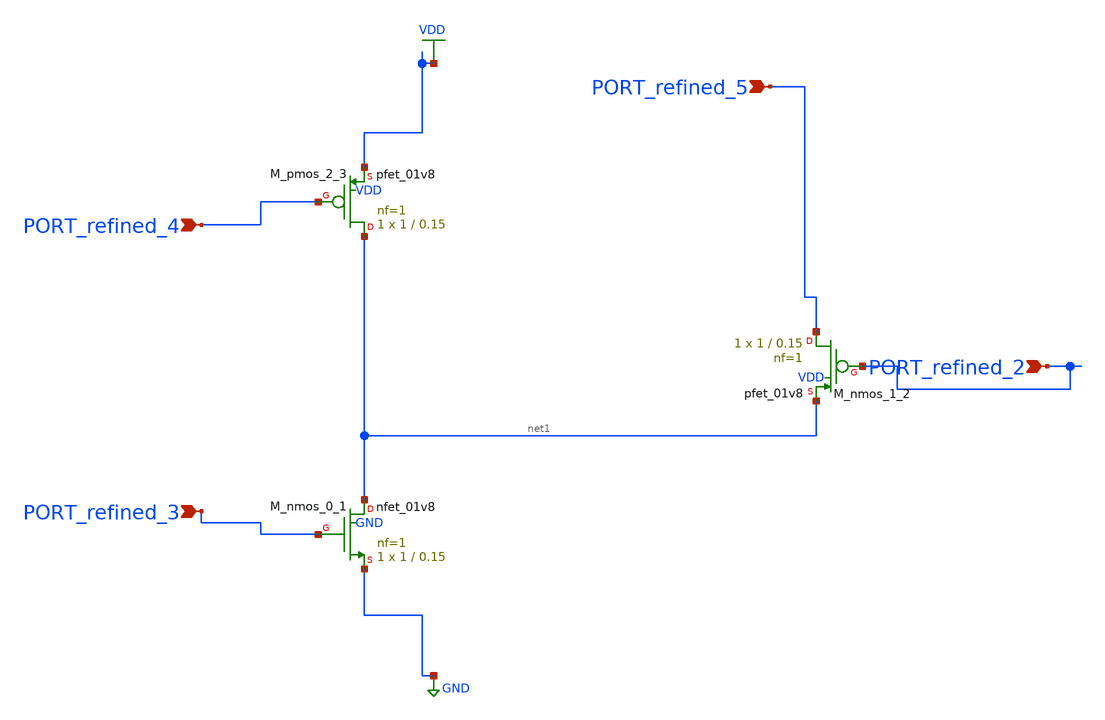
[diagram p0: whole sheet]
** sch_path: schematics/AMSNet/143.sch
**.subckt 143 PORT_refined_2 PORT_refined_3 PORT_refined_4 PORT_refined_5
*.ipin PORT_refined_2
*.ipin PORT_refined_3
*.ipin PORT_refined_4
*.ipin PORT_refined_5
XM_nmos_0_1 net1 PORT_refined_3 GND GND sky130_fd_pr__nfet_01v8 L=0.15 W=1 nf=1 ad='int((1 + 1)/2) * 1 / 1 * 0.29'
+ as='int((1 + 2)/2) * 1 / 1 * 0.29' pd='2*int((1 + 1)/2) * (1 / 1 + 0.29)' ps='2*int((1 + 2)/2) * (1 / 1 + 0.29)'
+ nrd='0.29 / 1 ' nrs='0.29 / 1 ' sa=0 sb=0 sd=0 mult=1 m=1
XM_nmos_1_2 PORT_refined_5 PORT_refined_2 net1 VDD sky130_fd_pr__pfet_01v8 L=0.15 W=1 nf=1 ad='int((1 + 1)/2) * 1 / 1 * 0.29'
+ as='int((1 + 2)/2) * 1 / 1 * 0.29' pd='2*int((1 + 1)/2) * (1 / 1 + 0.29)' ps='2*int((1 + 2)/2) * (1 / 1 + 0.29)'
+ nrd='0.29 / 1 ' nrs='0.29 / 1 ' sa=0 sb=0 sd=0 mult=1 m=1
XM_pmos_2_3 net1 PORT_refined_4 VDD VDD sky130_fd_pr__pfet_01v8 L=0.15 W=1 nf=1 ad='int((1 + 1)/2) * 1 / 1 * 0.29'
+ as='int((1 + 2)/2) * 1 / 1 * 0.29' pd='2*int((1 + 1)/2) * (1 / 1 + 0.29)' ps='2*int((1 + 2)/2) * (1 / 1 + 0.29)'
+ nrd='0.29 / 1 ' nrs='0.29 / 1 ' sa=0 sb=0 sd=0 mult=1 m=1
**.ends
.GLOBAL GND
.GLOBAL VDD
.end
